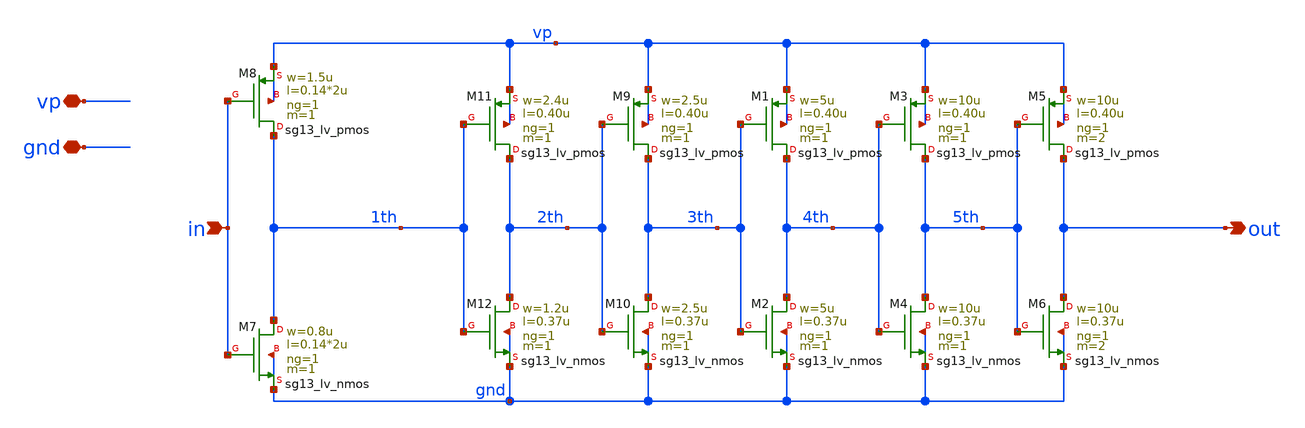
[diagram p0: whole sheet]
** sch_path: schematics/vco/vco_cell/0_buf.sch
**.subckt 0_buf in out vp gnd
*.ipin in
*.opin out
*.iopin vp
*.iopin gnd
XM9 3th 2th vp vp sg13_lv_pmos w=2.5u l=0.40u ng=1 m=1 mm_ok=1
XM10 3th 2th gnd gnd sg13_lv_nmos w=2.5u l=0.37u ng=1 m=1 mm_ok=1
XM11 2th 1th vp vp sg13_lv_pmos w=2.4u l=0.40u ng=1 m=1 mm_ok=1
XM12 2th 1th gnd gnd sg13_lv_nmos w=1.2u l=0.37u ng=1 m=1 mm_ok=1
XM1 4th 3th vp vp sg13_lv_pmos w=5u l=0.40u ng=1 m=1 mm_ok=1
XM2 4th 3th gnd gnd sg13_lv_nmos w=5u l=0.37u ng=1 m=1 mm_ok=1
XM3 5th 4th vp vp sg13_lv_pmos w=10u l=0.40u ng=1 m=1 mm_ok=1
XM4 5th 4th gnd gnd sg13_lv_nmos w=10u l=0.37u ng=1 m=1 mm_ok=1
XM5 out 5th vp vp sg13_lv_pmos w=10u l=0.40u ng=1 m=2 mm_ok=1
XM6 out 5th gnd gnd sg13_lv_nmos w=10u l=0.37u ng=1 m=2 mm_ok=1
XM7 1th in gnd gnd sg13_lv_nmos w=0.8u l=0.14*2u ng=1 m=1 mm_ok=1
XM8 1th in vp vp sg13_lv_pmos w=1.5u l=0.14*2u ng=1 m=1 mm_ok=1
**.ends
.end
